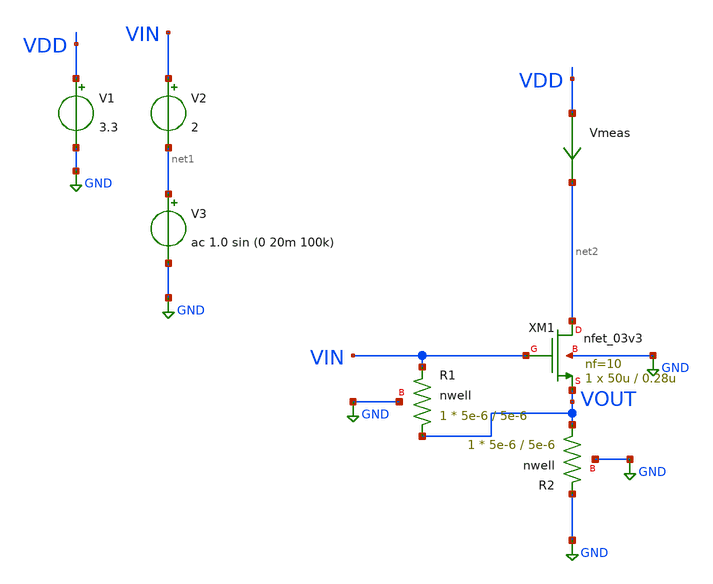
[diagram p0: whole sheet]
** sch_path: simple_amp6.sch
**.subckt simple_amp6
XM1 net2 VIN VOUT GND nfet_03v3 L=0.28u W=50u nf=10 ad='int((nf+1)/2) * W/nf * 0.18u' as='int((nf+2)/2) * W/nf * 0.18u'
+ pd='2*int((nf+1)/2) * (W/nf + 0.18u)' ps='2*int((nf+2)/2) * (W/nf + 0.18u)' nrd='0.18u / W' nrs='0.18u / W'
+ sa=0 sb=0 sd=0 m=1
Vmeas VDD net2 0
.save i(vmeas)
V1 VDD GND 3.3
V2 VIN net1 2
XR1 VOUT VIN GND nwell r_width=5e-6 r_length=5e-6 m=1
XR2 VOUT GND GND nwell r_width=5e-6 r_length=5e-6 m=1
V3 net1 GND ac 1.0 sin (0 20m 100k)
**** begin user architecture code

.include $::180MCU_MODELS/design.ngspice
*.lib $::180MCU_MODELS/sm141064.ngspice statistical
*.lib $::180MCU_MODELS/sm141064.ngspice res_statistical
.lib $::180MCU_MODELS/sm141064.ngspice typical
.lib $::180MCU_MODELS/sm141064.ngspice res_typical
.lib $::180MCU_MODELS/sm141064.ngspice moscap_typical
.lib $::180MCU_MODELS/sm141064.ngspice bjt_typical
.lib $::180MCU_MODELS/sm141064.ngspice diode_typical
.lib $::180MCU_MODELS/sm141064.ngspice mimcap_typical
.TEMP 27

.param   sw_stat_global = 1   sw_stat_mism = 1  mc_skew = 3  res_mc_skew = 3  cap_mc_skew = 3
+  fnoicor = 1



.control
save all
dc V2 0 3.3 0.01


plot v(VOUT) deriv(v(VOUT)) v(VIN) (v(VIN)-v(VOUT)) (v(VDD)-v(VOUT))
plot v(VOUT) deriv(v(VOUT))
plot i(Vmeas)
plot deriv(v(VOUT))
tran 10ns 20u
plot (v(VOUT)-1.14755) (v(VIN)-2)
plot fft((v(VOUT))) fft((v(VIN)))
ac dec 20 1 50G
plot v(VOUT)
.endc

**** end user architecture code
**.ends
.GLOBAL GND
.end
